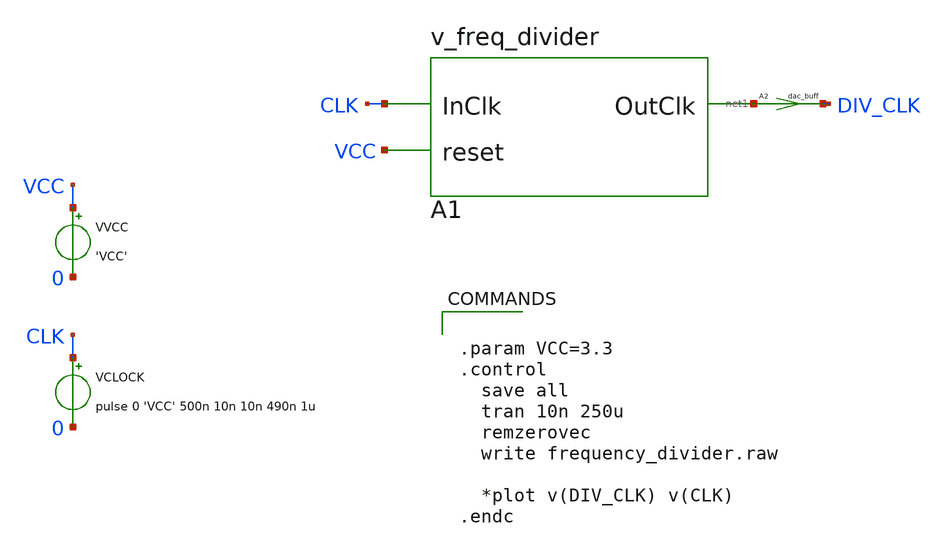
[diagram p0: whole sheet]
** sch_path: sch/tb/frequency_divider.sch
**.subckt frequency_divider
VVCC VCC 0 'VCC'
VCLOCK CLK 0 pulse 0 'VCC' 500n 10n 10n 490n 1u
A2 [ net1 ] [ DIV_CLK ] dac_buff
A1 [ CLK VCC ] [ net1 ] freq_divider
**** begin user architecture code


.param VCC=3.3
.control
  save all
  tran 10n 250u
  remzerovec
  write frequency_divider.raw

  *plot v(DIV_CLK) v(CLK)
.endc


**** end user architecture code
**.ends
**** begin user architecture code
.model dac_buff dac_bridge input_load=1e-15 t_rise=10n t_fall=10n  out_low=0 out_high=3.3
**** end user architecture code
.end
